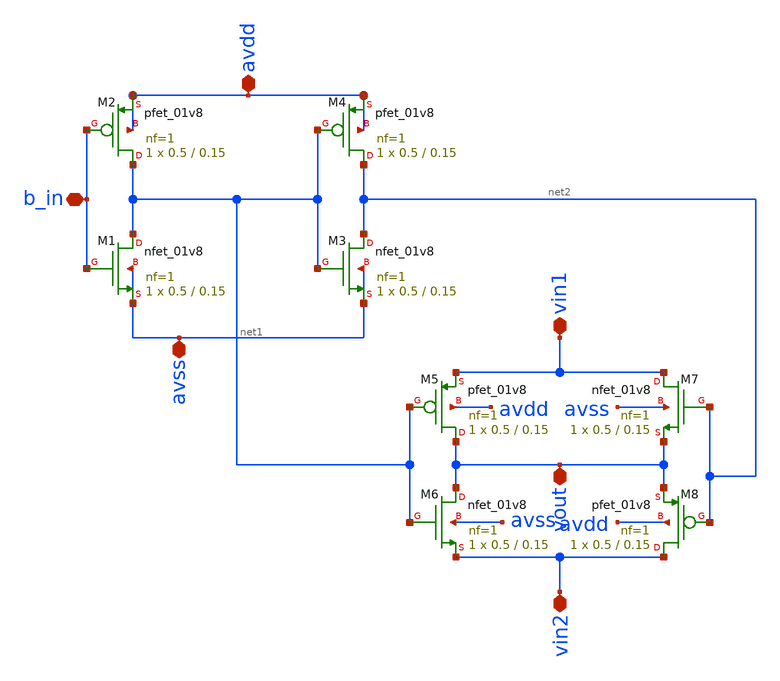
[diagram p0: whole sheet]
** sch_path: designs/libs/crossmem_ipn/dac4bits/sch/sw.sch
**.subckt sw avss vin1 vout avdd vin2 b_in
*.iopin avss
*.iopin vin1
*.iopin vout
*.iopin avdd
*.iopin vin2
*.iopin b_in
XM1 net1 b_in avss avss sky130_fd_pr__nfet_01v8 L=0.15 W=0.5 nf=1 ad='int((nf+1)/2) * W/nf * 0.29' as='int((nf+2)/2) * W/nf * 0.29'
+ pd='2*int((nf+1)/2) * (W/nf + 0.29)' ps='2*int((nf+2)/2) * (W/nf + 0.29)' nrd='0.29 / W' nrs='0.29 / W'
+ sa=0 sb=0 sd=0 mult=1 m=1
XM2 net1 b_in avdd avdd sky130_fd_pr__pfet_01v8 L=0.15 W=0.5 nf=1 ad='int((nf+1)/2) * W/nf * 0.29' as='int((nf+2)/2) * W/nf * 0.29'
+ pd='2*int((nf+1)/2) * (W/nf + 0.29)' ps='2*int((nf+2)/2) * (W/nf + 0.29)' nrd='0.29 / W' nrs='0.29 / W'
+ sa=0 sb=0 sd=0 mult=1 m=1
XM3 net2 net1 avss avss sky130_fd_pr__nfet_01v8 L=0.15 W=0.5 nf=1 ad='int((nf+1)/2) * W/nf * 0.29' as='int((nf+2)/2) * W/nf * 0.29'
+ pd='2*int((nf+1)/2) * (W/nf + 0.29)' ps='2*int((nf+2)/2) * (W/nf + 0.29)' nrd='0.29 / W' nrs='0.29 / W'
+ sa=0 sb=0 sd=0 mult=1 m=1
XM4 net2 net1 avdd avdd sky130_fd_pr__pfet_01v8 L=0.15 W=0.5 nf=1 ad='int((nf+1)/2) * W/nf * 0.29' as='int((nf+2)/2) * W/nf * 0.29'
+ pd='2*int((nf+1)/2) * (W/nf + 0.29)' ps='2*int((nf+2)/2) * (W/nf + 0.29)' nrd='0.29 / W' nrs='0.29 / W'
+ sa=0 sb=0 sd=0 mult=1 m=1
XM5 vout net1 vin1 avdd sky130_fd_pr__pfet_01v8 L=0.15 W=0.5 nf=1 ad='int((nf+1)/2) * W/nf * 0.29' as='int((nf+2)/2) * W/nf * 0.29'
+ pd='2*int((nf+1)/2) * (W/nf + 0.29)' ps='2*int((nf+2)/2) * (W/nf + 0.29)' nrd='0.29 / W' nrs='0.29 / W'
+ sa=0 sb=0 sd=0 mult=1 m=1
XM6 vout net1 vin2 avss sky130_fd_pr__nfet_01v8 L=0.15 W=0.5 nf=1 ad='int((nf+1)/2) * W/nf * 0.29' as='int((nf+2)/2) * W/nf * 0.29'
+ pd='2*int((nf+1)/2) * (W/nf + 0.29)' ps='2*int((nf+2)/2) * (W/nf + 0.29)' nrd='0.29 / W' nrs='0.29 / W'
+ sa=0 sb=0 sd=0 mult=1 m=1
XM7 vin1 net2 vout avss sky130_fd_pr__nfet_01v8 L=0.15 W=0.5 nf=1 ad='int((nf+1)/2) * W/nf * 0.29' as='int((nf+2)/2) * W/nf * 0.29'
+ pd='2*int((nf+1)/2) * (W/nf + 0.29)' ps='2*int((nf+2)/2) * (W/nf + 0.29)' nrd='0.29 / W' nrs='0.29 / W'
+ sa=0 sb=0 sd=0 mult=1 m=1
XM8 vin2 net2 vout avdd sky130_fd_pr__pfet_01v8 L=0.15 W=0.5 nf=1 ad='int((nf+1)/2) * W/nf * 0.29' as='int((nf+2)/2) * W/nf * 0.29'
+ pd='2*int((nf+1)/2) * (W/nf + 0.29)' ps='2*int((nf+2)/2) * (W/nf + 0.29)' nrd='0.29 / W' nrs='0.29 / W'
+ sa=0 sb=0 sd=0 mult=1 m=1
**.ends
.end
